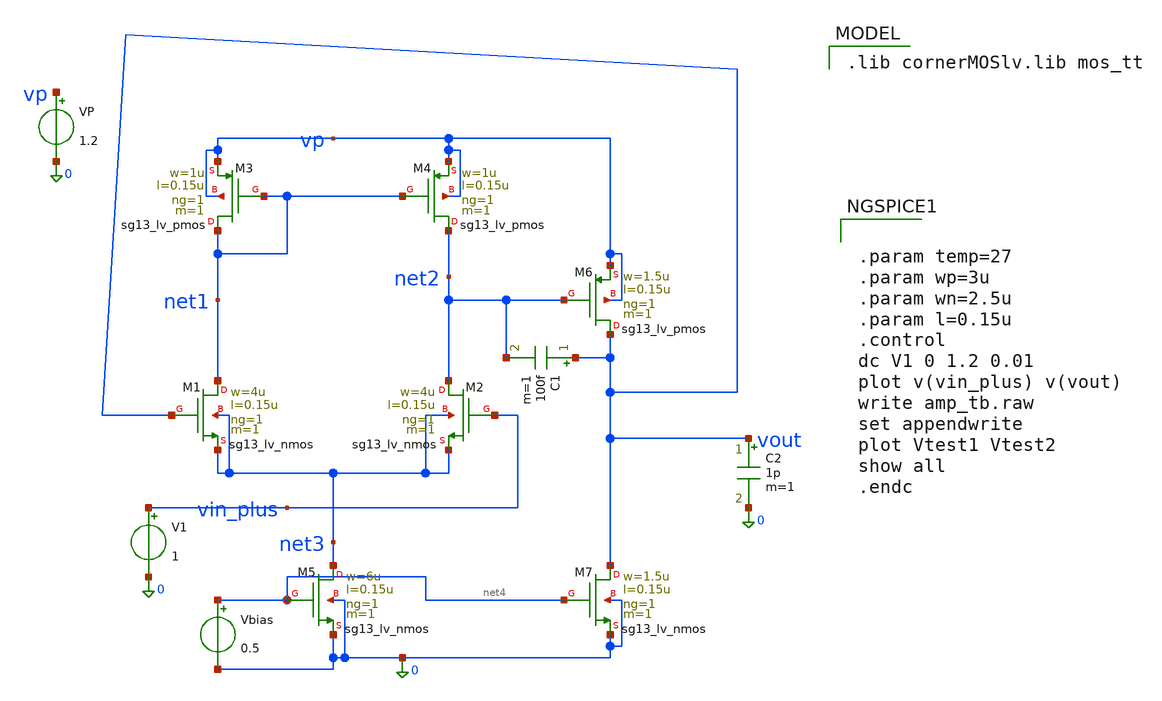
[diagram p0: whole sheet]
** sch_path: schematics/charge_pump/old_sch/amp_tb.sch
**.subckt amp_tb
VP vp 0 1.2
XM4 net2 net1 vp vp sg13_lv_pmos w=1u l=0.15u ng=1 m=1 mm_ok=1
XM1 net1 vout net3 net3 sg13_lv_nmos w=4u l=0.15u ng=1 m=1 mm_ok=1
XM3 net1 net1 vp vp sg13_lv_pmos w=1u l=0.15u ng=1 m=1 mm_ok=1
XM2 net2 vin_plus net3 net3 sg13_lv_nmos w=4u l=0.15u ng=1 m=1 mm_ok=1
XM5 net3 net4 0 0 sg13_lv_nmos w=6u l=0.15u ng=1 m=1 mm_ok=1
XM6 vout net2 vp vp sg13_lv_pmos w=1.5u l=0.15u ng=1 m=1 mm_ok=1
XM7 vout net4 0 0 sg13_lv_nmos w=1.5u l=0.15u ng=1 m=1 mm_ok=1
Vbias net4 0 0.5
C1 vout net2 100f m=1
C2 vout 0 1p m=1
V1 vin_plus 0 1
**** begin user architecture code
 .lib cornerMOSlv.lib mos_tt



.param temp=27
.param wp=3u
.param wn=2.5u
.param l=0.15u
.control
dc V1 0 1.2 0.01
plot v(vin_plus) v(vout)
write amp_tb.raw
set appendwrite
plot Vtest1 Vtest2
show all
.endc


**** end user architecture code
**.ends
.end
